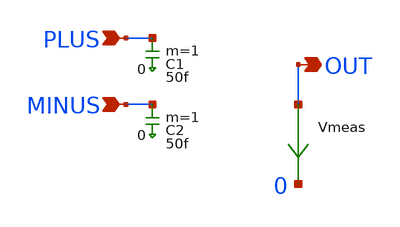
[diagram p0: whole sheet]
** sch_path: xschem-src/xschem_library/inst_sch_select/comp3_parax.sch
* Copyright (C) 1998-2026 Stefan Frederik Schippers
* This program is free software; you can redistribute it and/or modify
* it under the terms of the GNU General Public License as published by
* the Free Software Foundation; either version 2 of the License, or
* (at your option) any later version.
* This program is distributed in the hope that it will be useful,
* but WITHOUT ANY WARRANTY; without even the implied warranty of
* MERCHANTABILITY or FITNESS FOR A PARTICULAR PURPOSE.  See the
* GNU General Public License for more details.
* You should have received a copy of the GNU General Public License
* along with this program; if not, write to the Free Software
**.subckt comp3_parax OUT MINUS PLUS
*.opin OUT
*.ipin MINUS
*.ipin PLUS
C1 PLUS 0 50f m=1
C2 MINUS 0 50f m=1
Vmeas OUT 0 0
.save i(vmeas)
**.ends
.end
